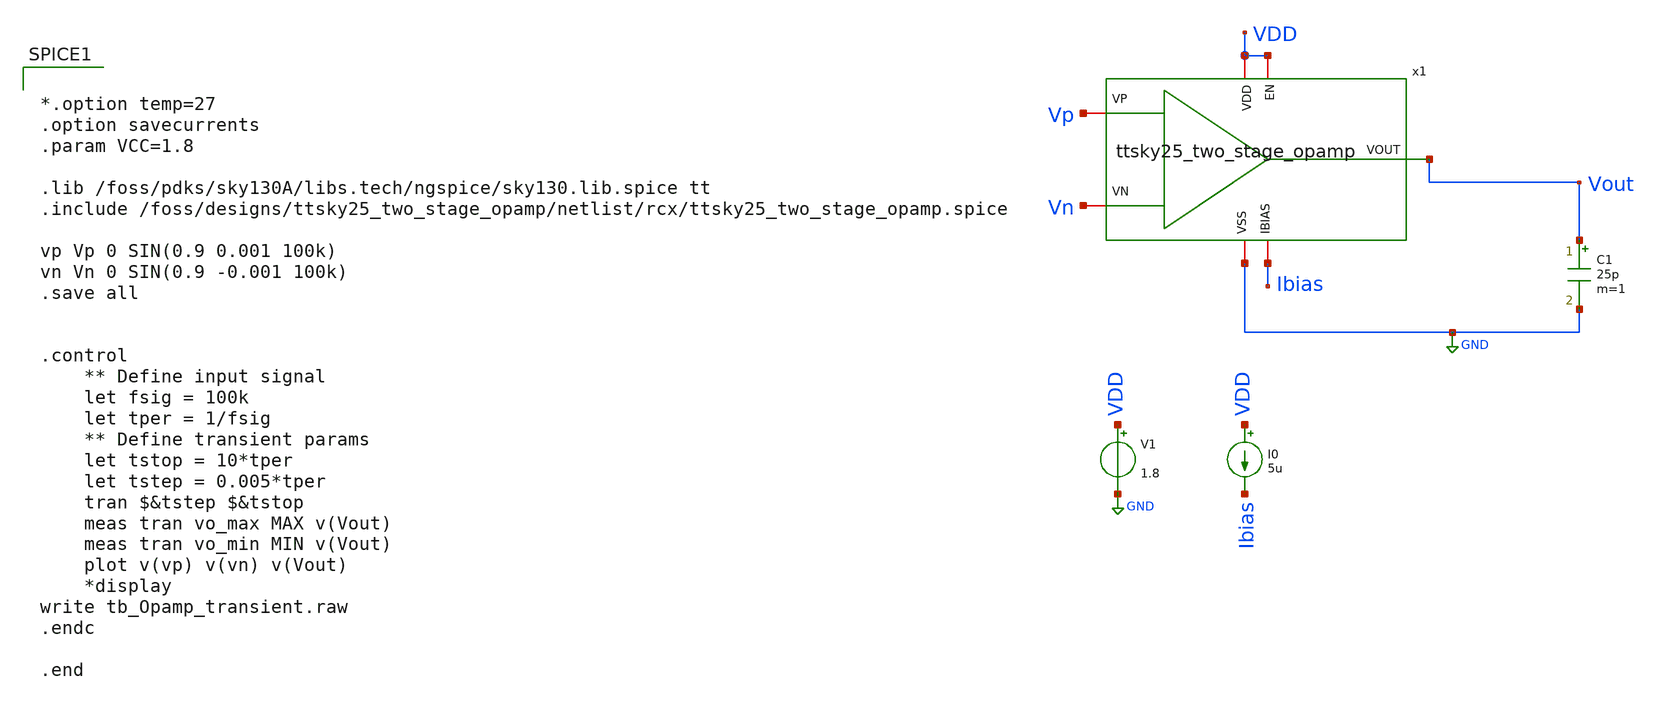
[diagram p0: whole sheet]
** sch_path: xschem/post-layout/testbenches/tb_Opamp_transient.sch
**.subckt tb_Opamp_transient
V1 VDD GND 1.8
I0 VDD Ibias 5u
C1 Vout GND 25p m=1
x1 VDD Ibias Vout Vn Vp VDD GND ttsky25_two_stage_opamp
**** begin user architecture code


*.option temp=27
.option savecurrents
.param VCC=1.8

.lib /foss/pdks/sky130A/libs.tech/ngspice/sky130.lib.spice tt
.include /foss/designs/ttsky25_two_stage_opamp/netlist/rcx/ttsky25_two_stage_opamp.spice

vp Vp 0 SIN(0.9 0.001 100k)
vn Vn 0 SIN(0.9 -0.001 100k)
.save all


.control
	** Define input signal
	let fsig = 100k
	let tper = 1/fsig
	** Define transient params
	let tstop = 10*tper
	let tstep = 0.005*tper
	tran $&tstep $&tstop
	meas tran vo_max MAX v(Vout)
	meas tran vo_min MIN v(Vout)
	plot v(vp) v(vn) v(Vout)
	*display
write tb_Opamp_transient.raw
.endc

.end


**** end user architecture code
**.ends
.GLOBAL GND
.end
